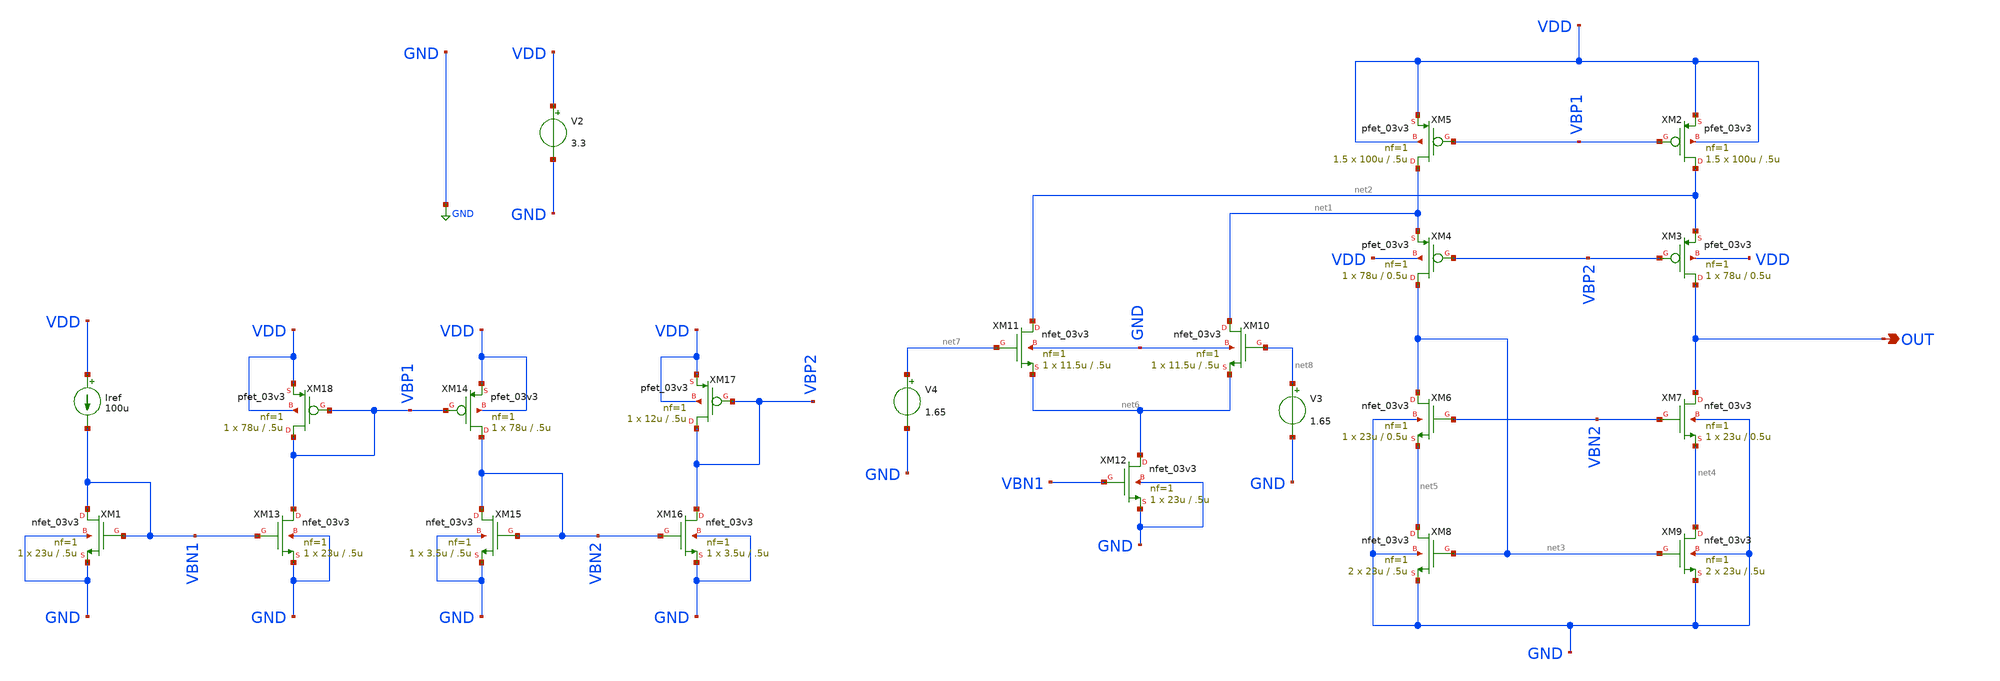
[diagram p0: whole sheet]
** sch_path: designs/libs/core_amps/ota_folded_cascode/folded_tb_schem.sch
**.subckt folded_tb_schem OUT
*.opin OUT
Iref VDD VBN1 100u
V2 VDD GND 3.3
XM1 VBN1 VBN1 GND GND nfet_03v3 L=.5u W=23u nf=1 ad='int((nf+1)/2) * W/nf * 0.18u' as='int((nf+2)/2) * W/nf * 0.18u'
+ pd='2*int((nf+1)/2) * (W/nf + 0.18u)' ps='2*int((nf+2)/2) * (W/nf + 0.18u)' nrd='0.18u / W' nrs='0.18u / W'
+ sa=0 sb=0 sd=0 m=1
XM2 net2 VBP1 VDD VDD pfet_03v3 L=.5u W=100u nf=1 ad='int((nf+1)/2) * W/nf * 0.18u' as='int((nf+2)/2) * W/nf * 0.18u'
+ pd='2*int((nf+1)/2) * (W/nf + 0.18u)' ps='2*int((nf+2)/2) * (W/nf + 0.18u)' nrd='0.18u / W' nrs='0.18u / W'
+ sa=0 sb=0 sd=0 m=1.5
XM3 OUT VBP2 net2 VDD pfet_03v3 L=0.5u W=78u nf=1 ad='int((nf+1)/2) * W/nf * 0.18u' as='int((nf+2)/2) * W/nf * 0.18u'
+ pd='2*int((nf+1)/2) * (W/nf + 0.18u)' ps='2*int((nf+2)/2) * (W/nf + 0.18u)' nrd='0.18u / W' nrs='0.18u / W'
+ sa=0 sb=0 sd=0 m=1
XM4 net3 VBP2 net1 VDD pfet_03v3 L=0.5u W=78u nf=1 ad='int((nf+1)/2) * W/nf * 0.18u' as='int((nf+2)/2) * W/nf * 0.18u'
+ pd='2*int((nf+1)/2) * (W/nf + 0.18u)' ps='2*int((nf+2)/2) * (W/nf + 0.18u)' nrd='0.18u / W' nrs='0.18u / W'
+ sa=0 sb=0 sd=0 m=1
XM5 net1 VBP1 VDD VDD pfet_03v3 L=.5u W=100u nf=1 ad='int((nf+1)/2) * W/nf * 0.18u' as='int((nf+2)/2) * W/nf * 0.18u'
+ pd='2*int((nf+1)/2) * (W/nf + 0.18u)' ps='2*int((nf+2)/2) * (W/nf + 0.18u)' nrd='0.18u / W' nrs='0.18u / W'
+ sa=0 sb=0 sd=0 m=1.5
XM6 net3 VBN2 net5 GND nfet_03v3 L=0.5u W=23u nf=1 ad='int((nf+1)/2) * W/nf * 0.18u' as='int((nf+2)/2) * W/nf * 0.18u'
+ pd='2*int((nf+1)/2) * (W/nf + 0.18u)' ps='2*int((nf+2)/2) * (W/nf + 0.18u)' nrd='0.18u / W' nrs='0.18u / W'
+ sa=0 sb=0 sd=0 m=1
XM7 OUT VBN2 net4 GND nfet_03v3 L=0.5u W=23u nf=1 ad='int((nf+1)/2) * W/nf * 0.18u' as='int((nf+2)/2) * W/nf * 0.18u'
+ pd='2*int((nf+1)/2) * (W/nf + 0.18u)' ps='2*int((nf+2)/2) * (W/nf + 0.18u)' nrd='0.18u / W' nrs='0.18u / W'
+ sa=0 sb=0 sd=0 m=1
XM8 net5 net3 GND GND nfet_03v3 L=.5u W=23u nf=1 ad='int((nf+1)/2) * W/nf * 0.18u' as='int((nf+2)/2) * W/nf * 0.18u'
+ pd='2*int((nf+1)/2) * (W/nf + 0.18u)' ps='2*int((nf+2)/2) * (W/nf + 0.18u)' nrd='0.18u / W' nrs='0.18u / W'
+ sa=0 sb=0 sd=0 m=2
XM9 net4 net3 GND GND nfet_03v3 L=.5u W=23u nf=1 ad='int((nf+1)/2) * W/nf * 0.18u' as='int((nf+2)/2) * W/nf * 0.18u'
+ pd='2*int((nf+1)/2) * (W/nf + 0.18u)' ps='2*int((nf+2)/2) * (W/nf + 0.18u)' nrd='0.18u / W' nrs='0.18u / W'
+ sa=0 sb=0 sd=0 m=2
XM10 net1 net8 net6 GND nfet_03v3 L=.5u W=11.5u nf=1 ad='int((nf+1)/2) * W/nf * 0.18u' as='int((nf+2)/2) * W/nf * 0.18u'
+ pd='2*int((nf+1)/2) * (W/nf + 0.18u)' ps='2*int((nf+2)/2) * (W/nf + 0.18u)' nrd='0.18u / W' nrs='0.18u / W'
+ sa=0 sb=0 sd=0 m=1
XM12 net6 VBN1 GND GND nfet_03v3 L=.5u W=23u nf=1 ad='int((nf+1)/2) * W/nf * 0.18u' as='int((nf+2)/2) * W/nf * 0.18u'
+ pd='2*int((nf+1)/2) * (W/nf + 0.18u)' ps='2*int((nf+2)/2) * (W/nf + 0.18u)' nrd='0.18u / W' nrs='0.18u / W'
+ sa=0 sb=0 sd=0 m=1
XM18 VBP1 VBP1 VDD VDD pfet_03v3 L=.5u W=78u nf=1 ad='int((nf+1)/2) * W/nf * 0.18u' as='int((nf+2)/2) * W/nf * 0.18u'
+ pd='2*int((nf+1)/2) * (W/nf + 0.18u)' ps='2*int((nf+2)/2) * (W/nf + 0.18u)' nrd='0.18u / W' nrs='0.18u / W'
+ sa=0 sb=0 sd=0 m=1
XM11 net2 net7 net6 GND nfet_03v3 L=.5u W=11.5u nf=1 ad='int((nf+1)/2) * W/nf * 0.18u' as='int((nf+2)/2) * W/nf * 0.18u'
+ pd='2*int((nf+1)/2) * (W/nf + 0.18u)' ps='2*int((nf+2)/2) * (W/nf + 0.18u)' nrd='0.18u / W' nrs='0.18u / W'
+ sa=0 sb=0 sd=0 m=1
V3 net8 GND 1.65
XM13 VBP1 VBN1 GND GND nfet_03v3 L=.5u W=23u nf=1 ad='int((nf+1)/2) * W/nf * 0.18u' as='int((nf+2)/2) * W/nf * 0.18u'
+ pd='2*int((nf+1)/2) * (W/nf + 0.18u)' ps='2*int((nf+2)/2) * (W/nf + 0.18u)' nrd='0.18u / W' nrs='0.18u / W'
+ sa=0 sb=0 sd=0 m=1
V4 net7 GND 1.65
XM14 VBN2 VBP1 VDD VDD pfet_03v3 L=.5u W=78u nf=1 ad='int((nf+1)/2) * W/nf * 0.18u' as='int((nf+2)/2) * W/nf * 0.18u'
+ pd='2*int((nf+1)/2) * (W/nf + 0.18u)' ps='2*int((nf+2)/2) * (W/nf + 0.18u)' nrd='0.18u / W' nrs='0.18u / W'
+ sa=0 sb=0 sd=0 m=1
XM15 VBN2 VBN2 GND GND nfet_03v3 L=.5u W=3.5u nf=1 ad='int((nf+1)/2) * W/nf * 0.18u' as='int((nf+2)/2) * W/nf * 0.18u'
+ pd='2*int((nf+1)/2) * (W/nf + 0.18u)' ps='2*int((nf+2)/2) * (W/nf + 0.18u)' nrd='0.18u / W' nrs='0.18u / W'
+ sa=0 sb=0 sd=0 m=1
XM16 VBP2 VBN2 GND GND nfet_03v3 L=.5u W=3.5u nf=1 ad='int((nf+1)/2) * W/nf * 0.18u' as='int((nf+2)/2) * W/nf * 0.18u'
+ pd='2*int((nf+1)/2) * (W/nf + 0.18u)' ps='2*int((nf+2)/2) * (W/nf + 0.18u)' nrd='0.18u / W' nrs='0.18u / W'
+ sa=0 sb=0 sd=0 m=1
XM17 VBP2 VBP2 VDD VDD pfet_03v3 L=.5u W=12u nf=1 ad='int((nf+1)/2) * W/nf * 0.18u' as='int((nf+2)/2) * W/nf * 0.18u'
+ pd='2*int((nf+1)/2) * (W/nf + 0.18u)' ps='2*int((nf+2)/2) * (W/nf + 0.18u)' nrd='0.18u / W' nrs='0.18u / W'
+ sa=0 sb=0 sd=0 m=1
**** begin user architecture code

.include $::180MCU_MODELS/design.ngspice
.lib $::180MCU_MODELS/sm141064.ngspice typical



.control
op

* --- key bias nodes (should be ~mid-supply / sane VGS) ---
print v(OUT) v(VBN1) v(VBP1)

print v(VBN2) v(VBP2)

print @m.xm11.m0[gm]


* --- gm/id on every device (target ~10) ---
let gmid_m1  = @m.xm1.m0[gm]/@m.xm1.m0[id]
let gmid_m2  = @m.xm2.m0[gm]/@m.xm2.m0[id]
let gmid_m3  = @m.xm3.m0[gm]/@m.xm3.m0[id]
let gmid_m4  = @m.xm4.m0[gm]/@m.xm4.m0[id]
let gmid_m5  = @m.xm5.m0[gm]/@m.xm5.m0[id]
let gmid_m6  = @m.xm6.m0[gm]/@m.xm6.m0[id]
let gmid_m7  = @m.xm7.m0[gm]/@m.xm7.m0[id]
let gmid_m8  = @m.xm8.m0[gm]/@m.xm8.m0[id]
let gmid_m9  = @m.xm9.m0[gm]/@m.xm9.m0[id]
let gmid_m10 = @m.xm10.m0[gm]/@m.xm10.m0[id]
let gmid_m11 = @m.xm11.m0[gm]/@m.xm11.m0[id]
let gmid_m12 = @m.xm12.m0[gm]/@m.xm12.m0[id]
let gmid_m13 = @m.xm13.m0[gm]/@m.xm13.m0[id]
let gmid_m18 = @m.xm18.m0[gm]/@m.xm18.m0[id]
print gmid_m1 gmid_m2 gmid_m3 gmid_m4 gmid_m5
print gmid_m6 gmid_m7 gmid_m8 gmid_m9 gmid_m10
print gmid_m11 gmid_m12 gmid_m13 gmid_m18

print @m.xm5.m0[id]
print @m.xm6.m0[id]
print @m.xm12.m0[id]
print @m.xm4.m0[id]

print @m.xm5.m0[vds]
print @m.xm2.m0[vds]
print @m.xm2.m0[vdsat]
print @m.xm5.m0[vdsat]

print @m.xm8.m0[vds]
print @m.xm9.m0[vds]
print @m.xm8.m0[vdsat]
print @m.xm9.m0[vdsat]

print @m.xm4.m0[vth]
print @m.xm6.m0[vth]


.endc


**** end user architecture code
**.ends
.GLOBAL GND
.end
